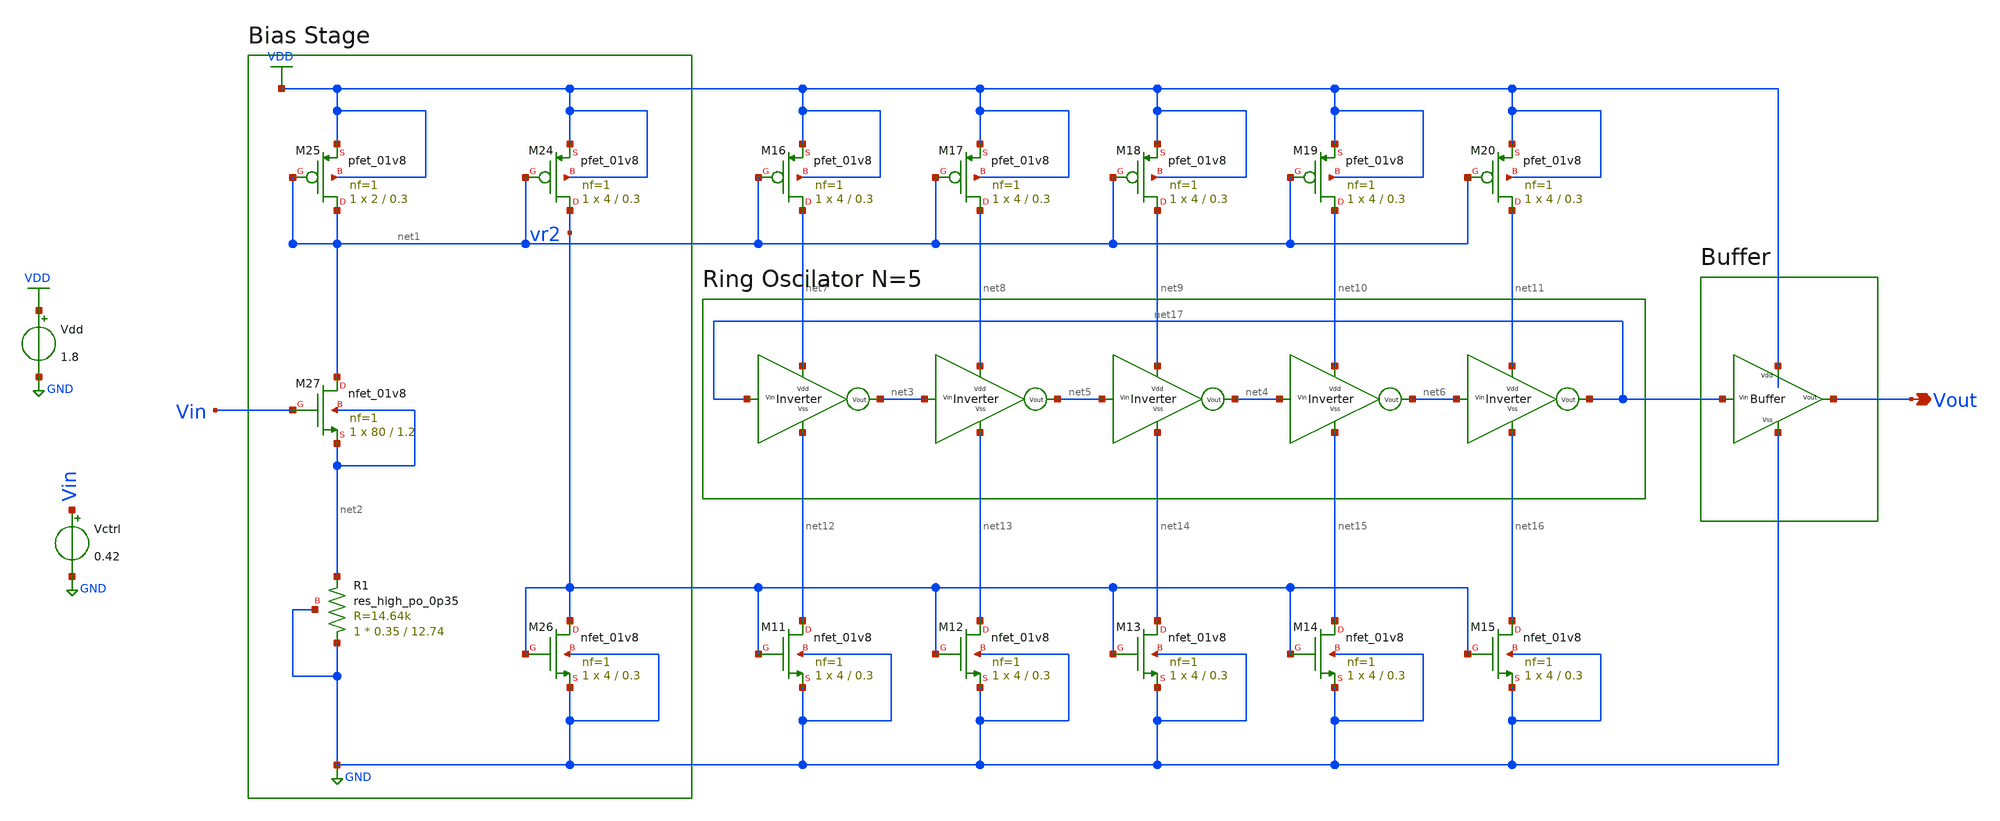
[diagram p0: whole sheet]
** sch_path: Current Starved VCO for PLL/xschem/CSVCO_v1.sch
**.subckt CSVCO_v1 Vout
*.opin Vout
XM27 net1 Vin net2 net2 sky130_fd_pr__nfet_01v8 L=1.2 W=80 nf=1 ad='int((nf+1)/2) * W/nf * 0.29' as='int((nf+2)/2) * W/nf * 0.29'
+ pd='2*int((nf+1)/2) * (W/nf + 0.29)' ps='2*int((nf+2)/2) * (W/nf + 0.29)' nrd='0.29 / W' nrs='0.29 / W'
+ sa=0 sb=0 sd=0 mult=1 m=1
XR1 GND net2 GND sky130_fd_pr__res_high_po_0p35 L=12.74 mult=1 m=1
XM26 vr2 vr2 GND GND sky130_fd_pr__nfet_01v8 L=0.3 W=4 nf=1 ad='int((nf+1)/2) * W/nf * 0.29' as='int((nf+2)/2) * W/nf * 0.29'
+ pd='2*int((nf+1)/2) * (W/nf + 0.29)' ps='2*int((nf+2)/2) * (W/nf + 0.29)' nrd='0.29 / W' nrs='0.29 / W'
+ sa=0 sb=0 sd=0 mult=1 m=1
XM25 net1 net1 VDD VDD sky130_fd_pr__pfet_01v8 L=0.3 W=2 nf=1 ad='int((nf+1)/2) * W/nf * 0.29' as='int((nf+2)/2) * W/nf * 0.29'
+ pd='2*int((nf+1)/2) * (W/nf + 0.29)' ps='2*int((nf+2)/2) * (W/nf + 0.29)' nrd='0.29 / W' nrs='0.29 / W'
+ sa=0 sb=0 sd=0 mult=1 m=1
XM24 vr2 net1 VDD VDD sky130_fd_pr__pfet_01v8 L=0.3 W=4 nf=1 ad='int((nf+1)/2) * W/nf * 0.29' as='int((nf+2)/2) * W/nf * 0.29'
+ pd='2*int((nf+1)/2) * (W/nf + 0.29)' ps='2*int((nf+2)/2) * (W/nf + 0.29)' nrd='0.29 / W' nrs='0.29 / W'
+ sa=0 sb=0 sd=0 mult=1 m=1
XM11 net12 vr2 GND GND sky130_fd_pr__nfet_01v8 L=0.3 W=4 nf=1 ad='int((nf+1)/2) * W/nf * 0.29' as='int((nf+2)/2) * W/nf * 0.29'
+ pd='2*int((nf+1)/2) * (W/nf + 0.29)' ps='2*int((nf+2)/2) * (W/nf + 0.29)' nrd='0.29 / W' nrs='0.29 / W'
+ sa=0 sb=0 sd=0 mult=1 m=1
XM12 net13 vr2 GND GND sky130_fd_pr__nfet_01v8 L=0.3 W=4 nf=1 ad='int((nf+1)/2) * W/nf * 0.29' as='int((nf+2)/2) * W/nf * 0.29'
+ pd='2*int((nf+1)/2) * (W/nf + 0.29)' ps='2*int((nf+2)/2) * (W/nf + 0.29)' nrd='0.29 / W' nrs='0.29 / W'
+ sa=0 sb=0 sd=0 mult=1 m=1
XM13 net14 vr2 GND GND sky130_fd_pr__nfet_01v8 L=0.3 W=4 nf=1 ad='int((nf+1)/2) * W/nf * 0.29' as='int((nf+2)/2) * W/nf * 0.29'
+ pd='2*int((nf+1)/2) * (W/nf + 0.29)' ps='2*int((nf+2)/2) * (W/nf + 0.29)' nrd='0.29 / W' nrs='0.29 / W'
+ sa=0 sb=0 sd=0 mult=1 m=1
XM14 net15 vr2 GND GND sky130_fd_pr__nfet_01v8 L=0.3 W=4 nf=1 ad='int((nf+1)/2) * W/nf * 0.29' as='int((nf+2)/2) * W/nf * 0.29'
+ pd='2*int((nf+1)/2) * (W/nf + 0.29)' ps='2*int((nf+2)/2) * (W/nf + 0.29)' nrd='0.29 / W' nrs='0.29 / W'
+ sa=0 sb=0 sd=0 mult=1 m=1
XM15 net16 vr2 GND GND sky130_fd_pr__nfet_01v8 L=0.3 W=4 nf=1 ad='int((nf+1)/2) * W/nf * 0.29' as='int((nf+2)/2) * W/nf * 0.29'
+ pd='2*int((nf+1)/2) * (W/nf + 0.29)' ps='2*int((nf+2)/2) * (W/nf + 0.29)' nrd='0.29 / W' nrs='0.29 / W'
+ sa=0 sb=0 sd=0 mult=1 m=1
XM16 net7 net1 VDD VDD sky130_fd_pr__pfet_01v8 L=0.3 W=4 nf=1 ad='int((nf+1)/2) * W/nf * 0.29' as='int((nf+2)/2) * W/nf * 0.29'
+ pd='2*int((nf+1)/2) * (W/nf + 0.29)' ps='2*int((nf+2)/2) * (W/nf + 0.29)' nrd='0.29 / W' nrs='0.29 / W'
+ sa=0 sb=0 sd=0 mult=1 m=1
XM17 net8 net1 VDD VDD sky130_fd_pr__pfet_01v8 L=0.3 W=4 nf=1 ad='int((nf+1)/2) * W/nf * 0.29' as='int((nf+2)/2) * W/nf * 0.29'
+ pd='2*int((nf+1)/2) * (W/nf + 0.29)' ps='2*int((nf+2)/2) * (W/nf + 0.29)' nrd='0.29 / W' nrs='0.29 / W'
+ sa=0 sb=0 sd=0 mult=1 m=1
XM18 net9 net1 VDD VDD sky130_fd_pr__pfet_01v8 L=0.3 W=4 nf=1 ad='int((nf+1)/2) * W/nf * 0.29' as='int((nf+2)/2) * W/nf * 0.29'
+ pd='2*int((nf+1)/2) * (W/nf + 0.29)' ps='2*int((nf+2)/2) * (W/nf + 0.29)' nrd='0.29 / W' nrs='0.29 / W'
+ sa=0 sb=0 sd=0 mult=1 m=1
XM19 net10 net1 VDD VDD sky130_fd_pr__pfet_01v8 L=0.3 W=4 nf=1 ad='int((nf+1)/2) * W/nf * 0.29' as='int((nf+2)/2) * W/nf * 0.29'
+ pd='2*int((nf+1)/2) * (W/nf + 0.29)' ps='2*int((nf+2)/2) * (W/nf + 0.29)' nrd='0.29 / W' nrs='0.29 / W'
+ sa=0 sb=0 sd=0 mult=1 m=1
XM20 net11 net1 VDD VDD sky130_fd_pr__pfet_01v8 L=0.3 W=4 nf=1 ad='int((nf+1)/2) * W/nf * 0.29' as='int((nf+2)/2) * W/nf * 0.29'
+ pd='2*int((nf+1)/2) * (W/nf + 0.29)' ps='2*int((nf+2)/2) * (W/nf + 0.29)' nrd='0.29 / W' nrs='0.29 / W'
+ sa=0 sb=0 sd=0 mult=1 m=1
x1 net7 net3 net17 net12 inverter
x2 net8 net5 net3 net13 inverter
x3 net9 net4 net5 net14 inverter
x4 net10 net6 net4 net15 inverter
x5 net11 net17 net6 net16 inverter
x6 VDD Vout net17 GND buffer
Vdd VDD GND 1.8
Vctrl Vin GND 0.42
**** begin user architecture code


.lib /foss/pdks/sky130A/libs.tech/ngspice/sky130.lib.spice tt
.control
tran 0.01n 2000n
plot V(Vout)
.endc


**** end user architecture code
**.ends

* expanding   symbol:  /foss/designs/campamento2023/inverter.sym # of pins=4
** sym_path: Current Starved VCO for PLL/xschem/inverter.sym
** sch_path: Current Starved VCO for PLL/xschem/inverter.sch
.subckt inverter Vdd Vout Vin Vss
*.iopin Vdd
*.opin Vout
*.iopin Vss
*.ipin Vin
XM1 Vout Vin Vss Vss sky130_fd_pr__nfet_01v8 L=0.45 W=2 nf=1 ad='int((nf+1)/2) * W/nf * 0.29' as='int((nf+2)/2) * W/nf * 0.29'
+ pd='2*int((nf+1)/2) * (W/nf + 0.29)' ps='2*int((nf+2)/2) * (W/nf + 0.29)' nrd='0.29 / W' nrs='0.29 / W'
+ sa=0 sb=0 sd=0 mult=1 m=1
XM2 Vout Vin Vdd Vdd sky130_fd_pr__pfet_01v8 L=0.45 W=4 nf=1 ad='int((nf+1)/2) * W/nf * 0.29' as='int((nf+2)/2) * W/nf * 0.29'
+ pd='2*int((nf+1)/2) * (W/nf + 0.29)' ps='2*int((nf+2)/2) * (W/nf + 0.29)' nrd='0.29 / W' nrs='0.29 / W'
+ sa=0 sb=0 sd=0 mult=1 m=1
.ends


* expanding   symbol:  /foss/designs/campamento2023/buffer.sym # of pins=4
** sym_path: Current Starved VCO for PLL/xschem/buffer.sym
** sch_path: Current Starved VCO for PLL/xschem/buffer.sch
.subckt buffer Vdd Vout Vin Vss
*.opin Vout
*.ipin Vin
*.iopin Vss
*.iopin Vdd
XM2 net1 Vin Vdd Vdd sky130_fd_pr__pfet_01v8 L=0.15 W=4 nf=1 ad='int((nf+1)/2) * W/nf * 0.29' as='int((nf+2)/2) * W/nf * 0.29'
+ pd='2*int((nf+1)/2) * (W/nf + 0.29)' ps='2*int((nf+2)/2) * (W/nf + 0.29)' nrd='0.29 / W' nrs='0.29 / W'
+ sa=0 sb=0 sd=0 mult=1 m=1
XM4 Vout net1 Vdd Vdd sky130_fd_pr__pfet_01v8 L=0.15 W=4 nf=1 ad='int((nf+1)/2) * W/nf * 0.29' as='int((nf+2)/2) * W/nf * 0.29'
+ pd='2*int((nf+1)/2) * (W/nf + 0.29)' ps='2*int((nf+2)/2) * (W/nf + 0.29)' nrd='0.29 / W' nrs='0.29 / W'
+ sa=0 sb=0 sd=0 mult=1 m=1
XM1 net1 Vin Vss Vss sky130_fd_pr__nfet_01v8 L=0.15 W=1 nf=1 ad='int((nf+1)/2) * W/nf * 0.29' as='int((nf+2)/2) * W/nf * 0.29'
+ pd='2*int((nf+1)/2) * (W/nf + 0.29)' ps='2*int((nf+2)/2) * (W/nf + 0.29)' nrd='0.29 / W' nrs='0.29 / W'
+ sa=0 sb=0 sd=0 mult=1 m=1
XM3 Vout net1 Vss Vss sky130_fd_pr__nfet_01v8 L=0.15 W=1 nf=1 ad='int((nf+1)/2) * W/nf * 0.29' as='int((nf+2)/2) * W/nf * 0.29'
+ pd='2*int((nf+1)/2) * (W/nf + 0.29)' ps='2*int((nf+2)/2) * (W/nf + 0.29)' nrd='0.29 / W' nrs='0.29 / W'
+ sa=0 sb=0 sd=0 mult=1 m=1
.ends

.GLOBAL VDD
.GLOBAL GND
.end
